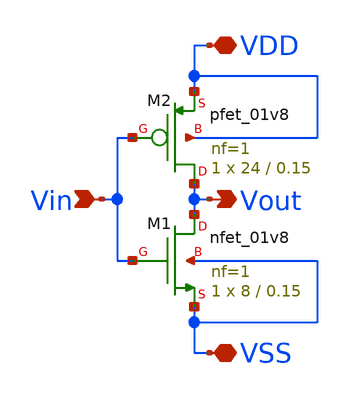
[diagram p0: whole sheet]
** sch_path: cmos_inverter/schematic/cmos_inverter.sch
**.subckt cmos_inverter Vin Vout VDD VSS
*.ipin Vin
*.opin Vout
*.iopin VDD
*.iopin VSS
XM1 Vout Vin VSS VSS sky130_fd_pr__nfet_01v8 L=0.15 W=8 nf=1 ad='int((1 + 1)/2) * 8 / 1 * 0.29' as='int((1 + 2)/2) * 8 / 1 * 0.29'
+ pd='2*int((1 + 1)/2) * (8 / 1 + 0.29)' ps='2*int((1 + 2)/2) * (8 / 1 + 0.29)' nrd='0.29 / 8 ' nrs='0.29 / 8 '
+ sa=0 sb=0 sd=0 mult=1 m=1
XM2 Vout Vin VDD VDD sky130_fd_pr__pfet_01v8 L=0.15 W=24 nf=1 ad='int((1 + 1)/2) * 24 / 1 * 0.29' as='int((1 + 2)/2) * 24 / 1 * 0.29'
+ pd='2*int((1 + 1)/2) * (24 / 1 + 0.29)' ps='2*int((1 + 2)/2) * (24 / 1 + 0.29)' nrd='0.29 / 24 ' nrs='0.29 / 24 '
+ sa=0 sb=0 sd=0 mult=1 m=1
**.ends
.end
